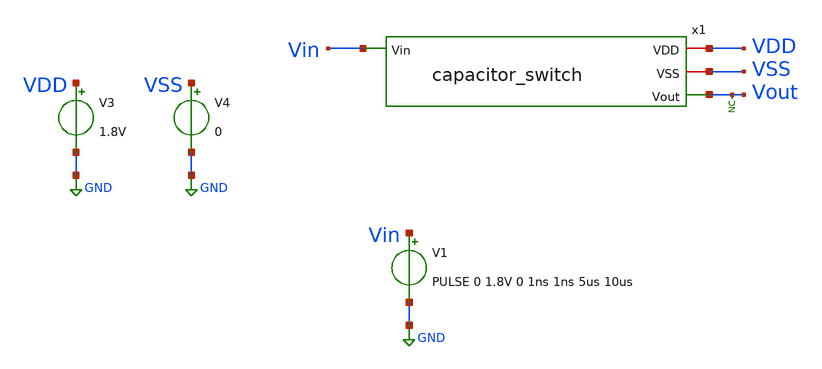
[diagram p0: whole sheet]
** sch_path: xschem/tests/capacitor_switch/capacitor_switch_test.sch
**.subckt capacitor_switch_test
V3 VDD GND 1.8V
V4 VSS GND 0
x1 VDD VSS Vout Vin capacitor_switch
V1 Vin GND PULSE 0 1.8V 0 1ns 1ns 5us 10us
* noconn Vout
**** begin user architecture code
 .lib $::SKYWATER_MODELS/sky130.lib.spice tt
.include $::SKYWATER_STDCELLS/sky130_fd_sc_hd.spice


.options acct list
.temp 25
*vvcc VDD 0 dc 1.8
*vvss VSS 0 0
.control
tran 0.1u 60u
*plot RST_PLS clk+2 Pulse+4
plot Vin Vout+2
write capacitor_switch_test.raw
.endc


**** end user architecture code
**.ends

* expanding   symbol:  src/capacitor_switch/capacitor_switch.sym # of pins=4
** sym_path: xschem/src/capacitor_switch/capacitor_switch.sym
** sch_path: xschem/src/capacitor_switch/capacitor_switch.sch
.subckt capacitor_switch VDD VSS Vout Vin
*.iopin VDD
*.ipin Vin
*.opin Vout
*.iopin VSS
XM1 net1 Vin VSS VSS sky130_fd_pr__nfet_01v8 L=0.15 W=0.910 nf=1 ad='int((nf+1)/2) * W/nf * 0.29' as='int((nf+2)/2) * W/nf * 0.29'
+ pd='2*int((nf+1)/2) * (W/nf + 0.29)' ps='2*int((nf+2)/2) * (W/nf + 0.29)' nrd='0.29 / W' nrs='0.29 / W'
+ sa=0 sb=0 sd=0 mult=1 m=1
XM2 net1 Vin VDD VDD sky130_fd_pr__pfet_01v8 L=0.15 W=1.650 nf=1 ad='int((nf+1)/2) * W/nf * 0.29' as='int((nf+2)/2) * W/nf * 0.29'
+ pd='2*int((nf+1)/2) * (W/nf + 0.29)' ps='2*int((nf+2)/2) * (W/nf + 0.29)' nrd='0.29 / W' nrs='0.29 / W'
+ sa=0 sb=0 sd=0 mult=1 m=1
XM3 Vout net1 VSS VSS sky130_fd_pr__nfet_01v8 L=0.15 W=0.910 nf=1 ad='int((nf+1)/2) * W/nf * 0.29' as='int((nf+2)/2) * W/nf * 0.29'
+ pd='2*int((nf+1)/2) * (W/nf + 0.29)' ps='2*int((nf+2)/2) * (W/nf + 0.29)' nrd='0.29 / W' nrs='0.29 / W'
+ sa=0 sb=0 sd=0 mult=50 m=50
XM4 Vout net1 VDD VDD sky130_fd_pr__pfet_01v8 L=0.15 W=1.650 nf=1 ad='int((nf+1)/2) * W/nf * 0.29' as='int((nf+2)/2) * W/nf * 0.29'
+ pd='2*int((nf+1)/2) * (W/nf + 0.29)' ps='2*int((nf+2)/2) * (W/nf + 0.29)' nrd='0.29 / W' nrs='0.29 / W'
+ sa=0 sb=0 sd=0 mult=50 m=50
.ends

.GLOBAL GND
.end
